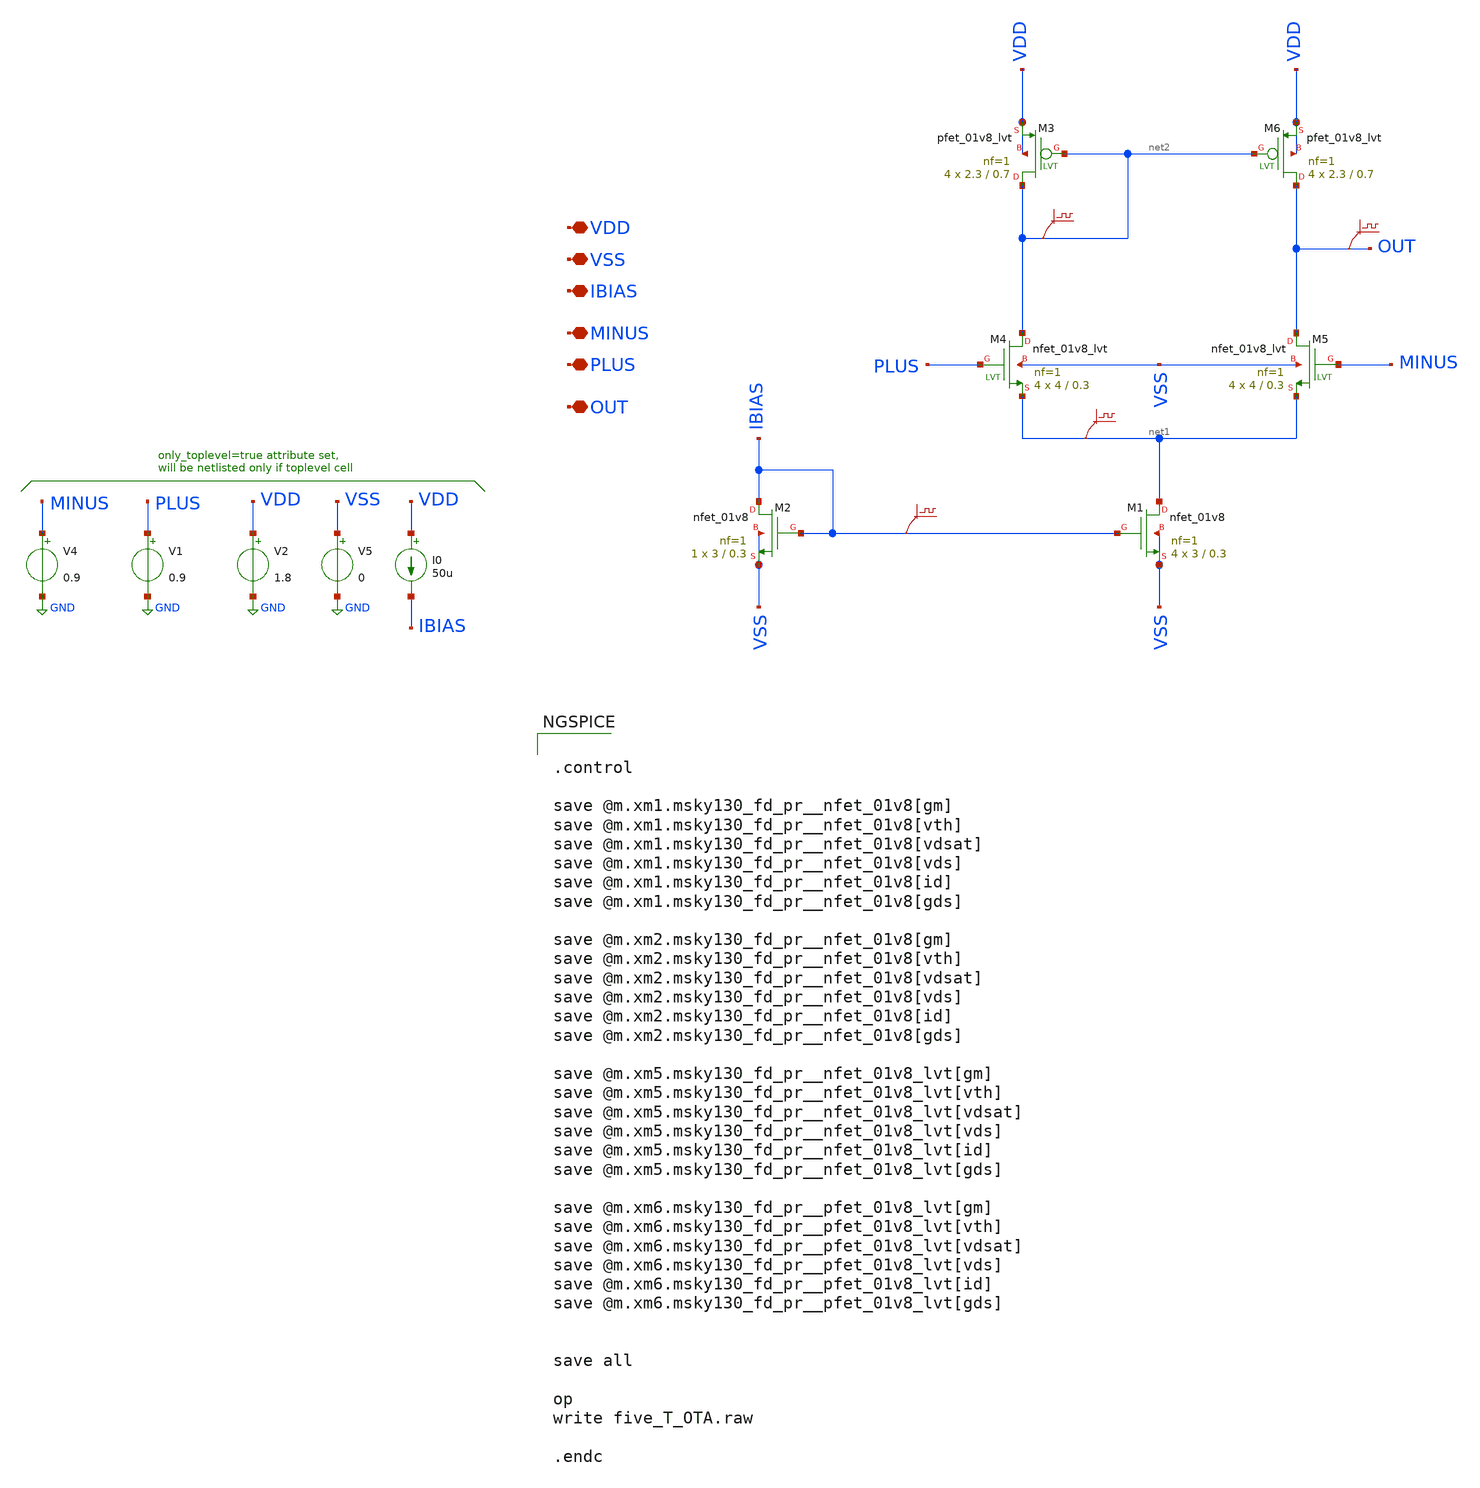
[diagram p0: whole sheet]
** sch_path: examples/xschem/five_T_OTA.sch
**.subckt five_T_OTA VDD VSS MINUS PLUS OUT IBIAS
*.iopin VDD
*.iopin VSS
*.iopin MINUS
*.iopin PLUS
*.iopin OUT
*.iopin IBIAS
V1 PLUS GND 0.9
V4 MINUS GND 0.9
V5 VSS GND 0
I0 VDD IBIAS 50u
XM2 IBIAS IBIAS VSS VSS sky130_fd_pr__nfet_01v8 L=0.3 W=3 nf=1 ad='int((nf+1)/2) * W/nf * 0.29' as='int((nf+2)/2) * W/nf * 0.29'
+ pd='2*int((nf+1)/2) * (W/nf + 0.29)' ps='2*int((nf+2)/2) * (W/nf + 0.29)' nrd='0.29 / W' nrs='0.29 / W'
+ sa=0 sb=0 sd=0 mult=1 m=1
XM1 net1 IBIAS VSS VSS sky130_fd_pr__nfet_01v8 L=0.3 W=3 nf=1 ad='int((nf+1)/2) * W/nf * 0.29' as='int((nf+2)/2) * W/nf * 0.29'
+ pd='2*int((nf+1)/2) * (W/nf + 0.29)' ps='2*int((nf+2)/2) * (W/nf + 0.29)' nrd='0.29 / W' nrs='0.29 / W'
+ sa=0 sb=0 sd=0 mult=4 m=4
.save v(ibias)
V2 VDD GND 1.8
.save v(out)
.save v(net2)
.save v(net1)
XM4 net2 PLUS net1 VSS sky130_fd_pr__nfet_01v8_lvt L=0.3 W=4 nf=1 ad='int((nf+1)/2) * W/nf * 0.29' as='int((nf+2)/2) * W/nf * 0.29'
+ pd='2*int((nf+1)/2) * (W/nf + 0.29)' ps='2*int((nf+2)/2) * (W/nf + 0.29)' nrd='0.29 / W' nrs='0.29 / W'
+ sa=0 sb=0 sd=0 mult=4 m=4
XM5 OUT MINUS net1 VSS sky130_fd_pr__nfet_01v8_lvt L=0.3 W=4 nf=1 ad='int((nf+1)/2) * W/nf * 0.29' as='int((nf+2)/2) * W/nf * 0.29'
+ pd='2*int((nf+1)/2) * (W/nf + 0.29)' ps='2*int((nf+2)/2) * (W/nf + 0.29)' nrd='0.29 / W' nrs='0.29 / W'
+ sa=0 sb=0 sd=0 mult=4 m=4
XM3 net2 net2 VDD VDD sky130_fd_pr__pfet_01v8_lvt L=0.7 W=2.3 nf=1 ad='int((nf+1)/2) * W/nf * 0.29' as='int((nf+2)/2) * W/nf * 0.29'
+ pd='2*int((nf+1)/2) * (W/nf + 0.29)' ps='2*int((nf+2)/2) * (W/nf + 0.29)' nrd='0.29 / W' nrs='0.29 / W'
+ sa=0 sb=0 sd=0 mult=4 m=4
XM6 OUT net2 VDD VDD sky130_fd_pr__pfet_01v8_lvt L=0.7 W=2.3 nf=1 ad='int((nf+1)/2) * W/nf * 0.29' as='int((nf+2)/2) * W/nf * 0.29'
+ pd='2*int((nf+1)/2) * (W/nf + 0.29)' ps='2*int((nf+2)/2) * (W/nf + 0.29)' nrd='0.29 / W' nrs='0.29 / W'
+ sa=0 sb=0 sd=0 mult=4 m=4
**** begin user architecture code

** opencircuitdesign pdks install
.lib $::SKYWATER_MODELS/sky130.lib.spice tt




.control

save @m.xm1.msky130_fd_pr__nfet_01v8[gm]
save @m.xm1.msky130_fd_pr__nfet_01v8[vth]
save @m.xm1.msky130_fd_pr__nfet_01v8[vdsat]
save @m.xm1.msky130_fd_pr__nfet_01v8[vds]
save @m.xm1.msky130_fd_pr__nfet_01v8[id]
save @m.xm1.msky130_fd_pr__nfet_01v8[gds]

save @m.xm2.msky130_fd_pr__nfet_01v8[gm]
save @m.xm2.msky130_fd_pr__nfet_01v8[vth]
save @m.xm2.msky130_fd_pr__nfet_01v8[vdsat]
save @m.xm2.msky130_fd_pr__nfet_01v8[vds]
save @m.xm2.msky130_fd_pr__nfet_01v8[id]
save @m.xm2.msky130_fd_pr__nfet_01v8[gds]

save @m.xm5.msky130_fd_pr__nfet_01v8_lvt[gm]
save @m.xm5.msky130_fd_pr__nfet_01v8_lvt[vth]
save @m.xm5.msky130_fd_pr__nfet_01v8_lvt[vdsat]
save @m.xm5.msky130_fd_pr__nfet_01v8_lvt[vds]
save @m.xm5.msky130_fd_pr__nfet_01v8_lvt[id]
save @m.xm5.msky130_fd_pr__nfet_01v8_lvt[gds]

save @m.xm6.msky130_fd_pr__pfet_01v8_lvt[gm]
save @m.xm6.msky130_fd_pr__pfet_01v8_lvt[vth]
save @m.xm6.msky130_fd_pr__pfet_01v8_lvt[vdsat]
save @m.xm6.msky130_fd_pr__pfet_01v8_lvt[vds]
save @m.xm6.msky130_fd_pr__pfet_01v8_lvt[id]
save @m.xm6.msky130_fd_pr__pfet_01v8_lvt[gds]


save all

op
write five_T_OTA.raw

.endc


**** end user architecture code
**.ends
.GLOBAL GND
.end
